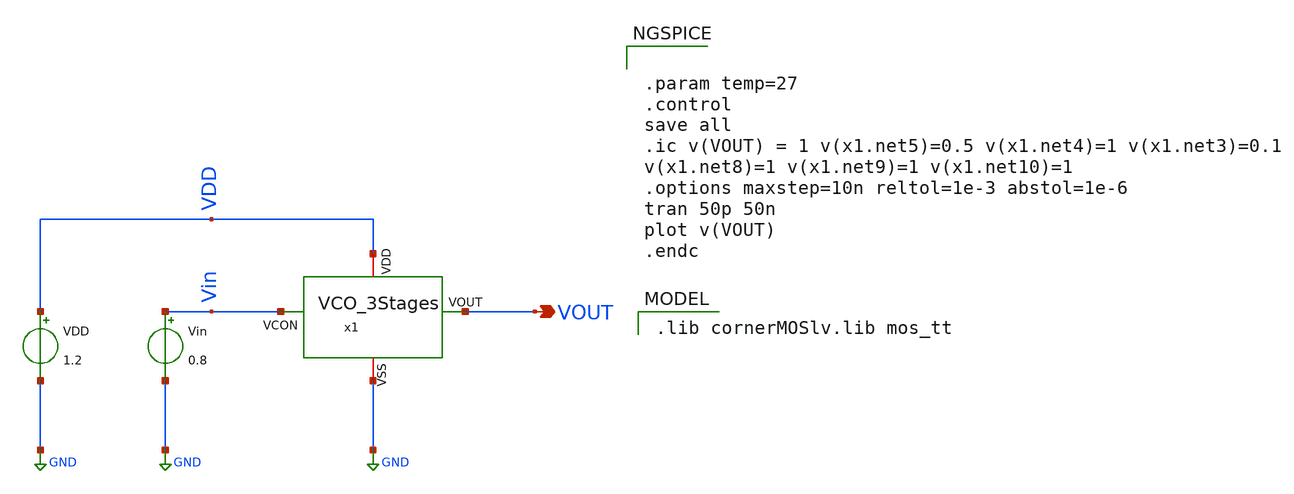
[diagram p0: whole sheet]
** sch_path: Team 1 Design/design_data/xschem/VCO/VCO_3Stages_tb.sch
**.subckt VCO_3Stages_tb VOUT
*.opin VOUT
VDD VDD GND 1.2
Vin Vin GND 0.8
x1 VDD VOUT Vin GND VCO_3Stages
**** begin user architecture code


.param temp=27
.control
save all
.ic v(VOUT) = 1 v(x1.net5)=0.5 v(x1.net4)=1 v(x1.net3)=0.1
v(x1.net8)=1 v(x1.net9)=1 v(x1.net10)=1
.options maxstep=10n reltol=1e-3 abstol=1e-6
tran 50p 50n
plot v(VOUT)
.endc


 .lib cornerMOSlv.lib mos_tt

**** end user architecture code
**.ends
.GLOBAL GND
.end
